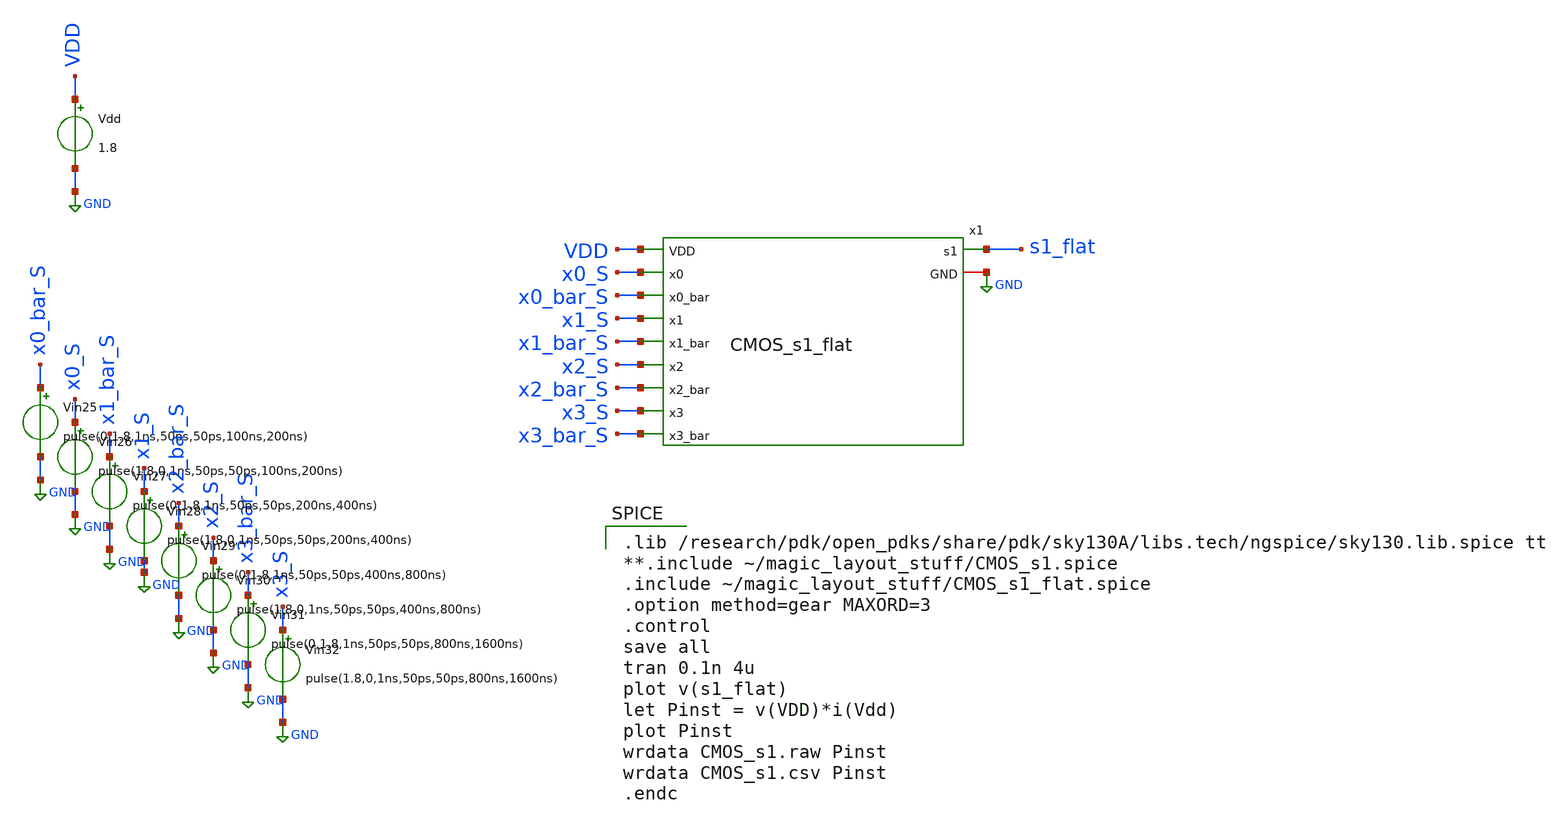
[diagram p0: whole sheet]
** sch_path: skywater_stuff/CMOS_s1_sim.sch
**.subckt CMOS_s1_sim
Vdd VDD GND 1.8
Vin25 x0_bar_S GND pulse(0,1.8,1ns,50ps,50ps,100ns,200ns)
Vin26 x0_S GND pulse(1.8,0,1ns,50ps,50ps,100ns,200ns)
Vin27 x1_bar_S GND pulse(0,1.8,1ns,50ps,50ps,200ns,400ns)
Vin28 x1_S GND pulse(1.8,0,1ns,50ps,50ps,200ns,400ns)
Vin29 x2_bar_S GND pulse(0,1.8,1ns,50ps,50ps,400ns,800ns)
Vin30 x2_S GND pulse(1.8,0,1ns,50ps,50ps,400ns,800ns)
Vin31 x3_bar_S GND pulse(0,1.8,1ns,50ps,50ps,800ns,1600ns)
Vin32 x3_S GND pulse(1.8,0,1ns,50ps,50ps,800ns,1600ns)
x1 GND x0_S x0_bar_S x1_S x1_bar_S x2_S x2_bar_S x3_S x3_bar_S s1_flat VDD CMOS_s1_flat
**** begin user architecture code

.lib /research/pdk/open_pdks/share/pdk/sky130A/libs.tech/ngspice/sky130.lib.spice tt
**.include ~/magic_layout_stuff/CMOS_s1.spice
.include ~/magic_layout_stuff/CMOS_s1_flat.spice
.option method=gear MAXORD=3
.control
save all
tran 0.1n 4u
plot v(s1_flat)
let Pinst = v(VDD)*i(Vdd)
plot Pinst
wrdata CMOS_s1.raw Pinst
wrdata CMOS_s1.csv Pinst
.endc


**** end user architecture code
**.ends
.GLOBAL GND
.end
